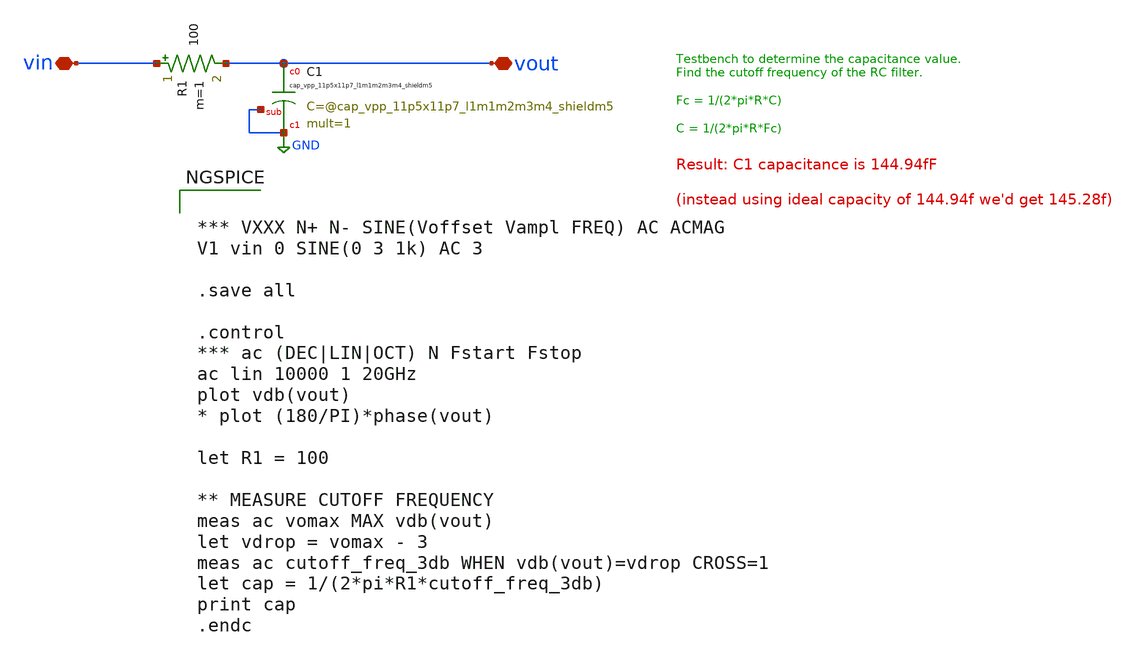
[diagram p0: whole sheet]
** sch_path: testdata/designs/sky130A/cap_vpp_11p5x11p7_l1m1m2m3m4_shieldm5/cap_vpp_11p5x11p7_l1m1m2m3m4_shieldm5_tb.sch
**.subckt cap_vpp_11p5x11p7_l1m1m2m3m4_shieldm5_tb vin vout
*.iopin vin
*.iopin vout
XC1 vout GND GND sky130_fd_pr__cap_vpp_11p5x11p7_l1m1m2m3m4_shieldm5 mult=1 m=1
R1 vin vout 100 m=1
**** begin user architecture code


*** VXXX N+ N- SINE(Voffset Vampl FREQ) AC ACMAG
V1 vin 0 SINE(0 3 1k) AC 3

.save all

.control
*** ac (DEC|LIN|OCT) N Fstart Fstop
ac lin 10000 1 20GHz
plot vdb(vout)
* plot (180/PI)*phase(vout)

let R1 = 100

** MEASURE CUTOFF FREQUENCY
meas ac vomax MAX vdb(vout)
let vdrop = vomax - 3
meas ac cutoff_freq_3db WHEN vdb(vout)=vdrop CROSS=1
let cap = 1/(2*pi*R1*cutoff_freq_3db)
print cap
.endc



** opencircuitdesign pdks install
.lib $::SKYWATER_MODELS/sky130.lib.spice tt


**** end user architecture code
**.ends
.GLOBAL GND
.end
